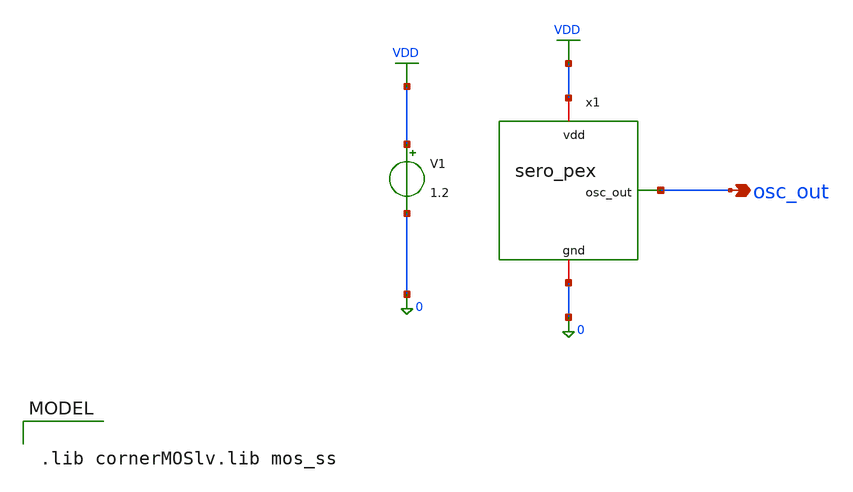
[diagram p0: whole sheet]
** sch_path: simulations/tb/tran_sero_pex.sch
**.subckt tran_sero_pex osc_out
*.opin osc_out
V1 VDD 0 1.2
x1 VDD osc_out 0 sero_pex
**** begin user architecture code

.lib cornerMOSlv.lib mos_ss



.param temp=27
.control
  save all
  tran 2p 10n

  display

  meas tran t1 when v(osc_out)=0.6 rise=3
  meas tran t2 when v(osc_out)=0.6 rise=4
  let freq = 1 / (t2 - t1)

  echo "========================================================================"
  echo "                SINGLE RUN TRANSIENT PERFORMANCE METRICS                "
  echo "========================================================================"
  print freq
  echo "========================================================================"

  write tran_sero_pex.raw
.endc


**** end user architecture code
**.ends

* expanding   symbol:  /foss/designs/sero/design/symbol/sero_pex.sym # of pins=3
** sym_path: design/symbol/sero.sym
.include /foss/designs/sero/simulations/pex/sero_lyt.pex.spice
.GLOBAL VDD
.end
